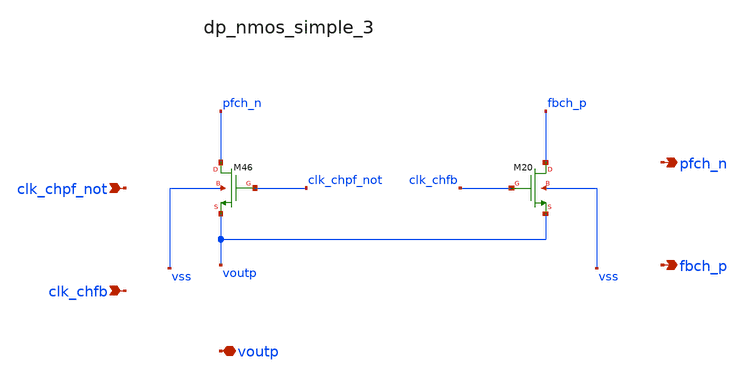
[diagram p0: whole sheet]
** sch_path: analog-db/raw/ia_003_fan_chopper_pf/hier/blocks/dp_nmos_simple_3.sch
**.subckt dp_nmos_simple_3 clk_chpf_not clk_chfb voutp pfch_n fbch_p
*.ipin clk_chpf_not
*.ipin clk_chfb
*.iopin voutp
*.opin pfch_n
*.opin fbch_p
XM20 fbch_p clk_chfb voutp vss sg13_lv_nmos w=x_dut_xm20_w l=x_dut_xm20_l ng=1 m=x_dut_xm20_m
XM46 pfch_n clk_chpf_not voutp vss sg13_lv_nmos w=x_dut_xm46_w l=x_dut_xm46_l ng=1 m=x_dut_xm46_m
**.ends
.end
